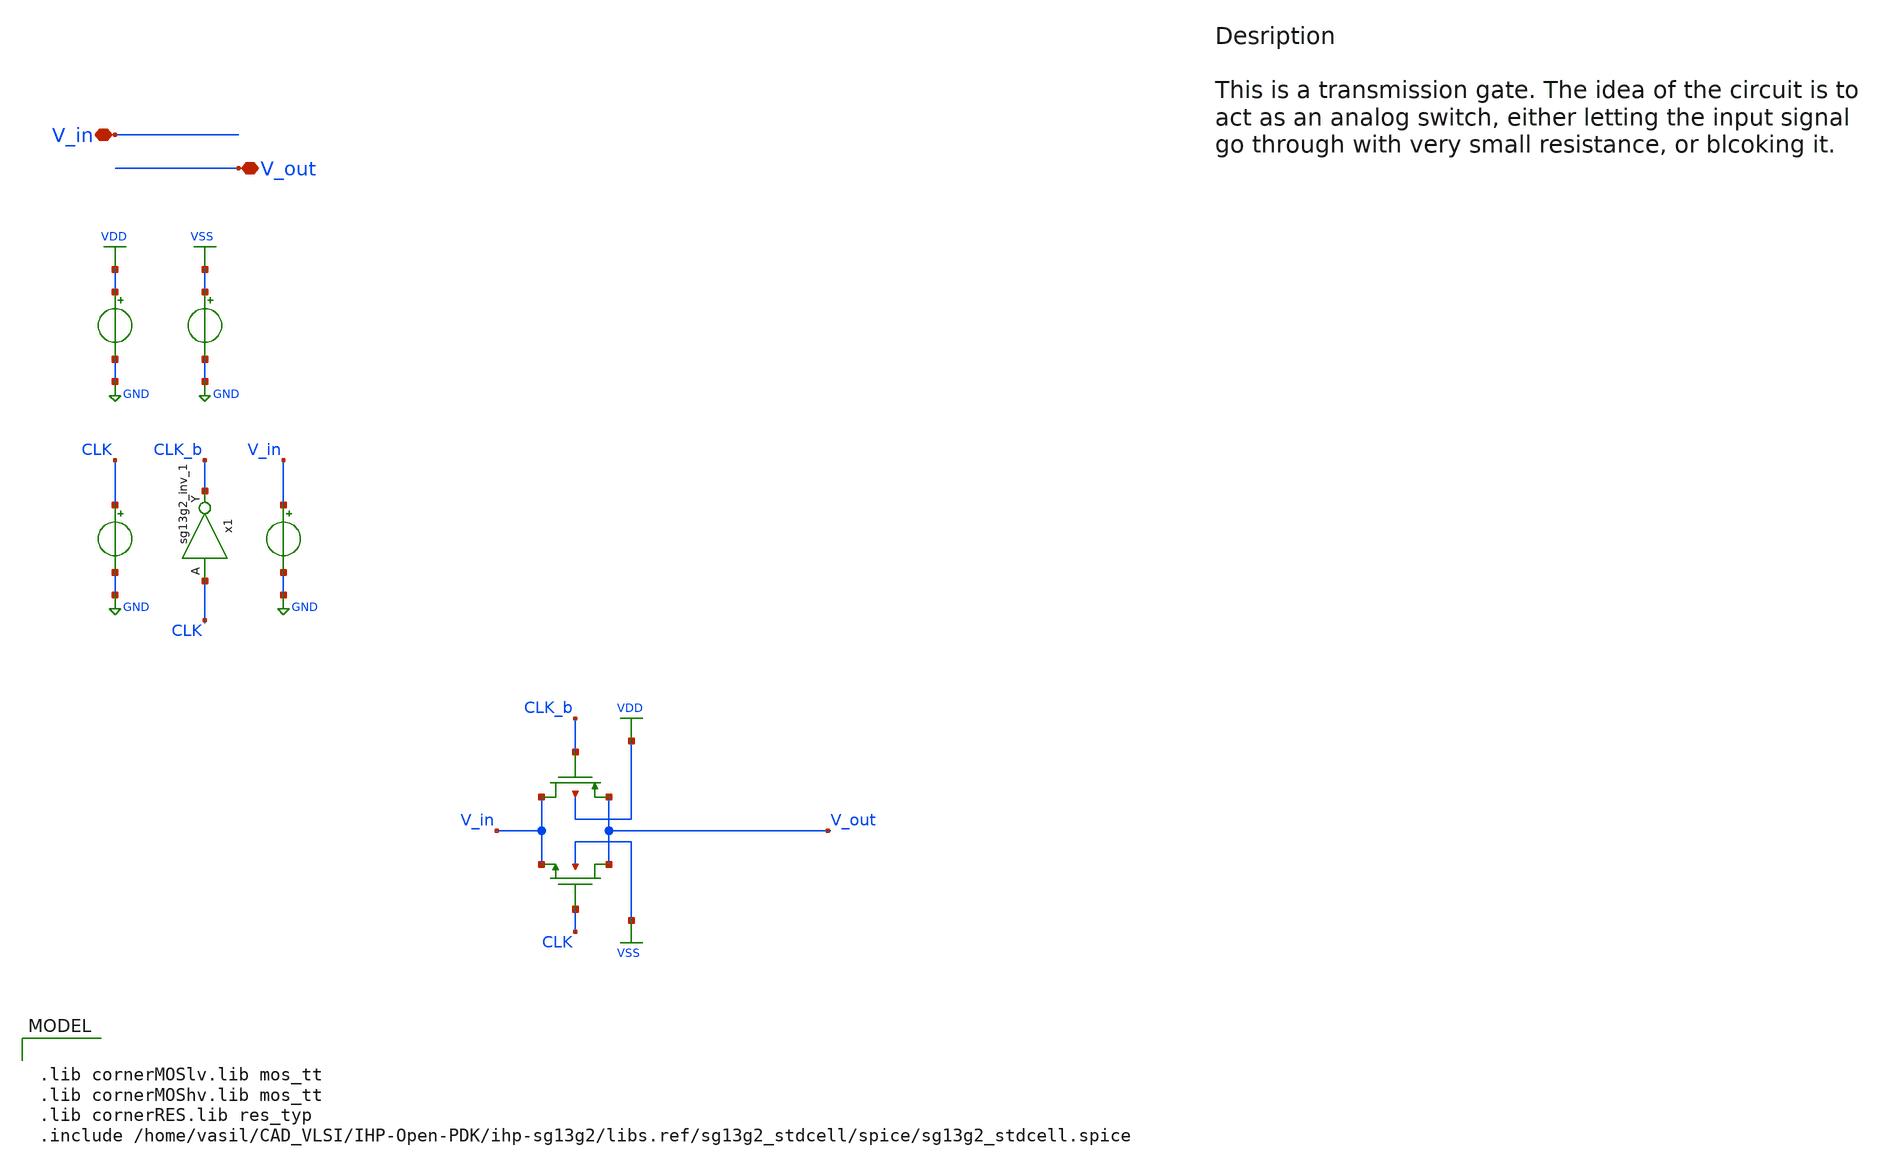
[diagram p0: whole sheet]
** sch_path: CKT_14/xschem/circuit_14.sch
**.subckt circuit_14 V_in V_out
*.iopin V_in
*.iopin V_out
XM1 V_in CLK_b V_out VDD sg13_lv_pmos w=1.0u l=0.45u ng=1 m=1 mm_ok=1
XM2 V_out CLK V_in VSS sg13_lv_nmos w=1.0u l=0.45u ng=1 m=1 mm_ok=1
V1 CLK GND pulse (0 1.5 0.5n 100p 100p 1n 2.2n)
.save i(v1)
V2 VDD GND 1.5
.save i(v2)
V3 VSS GND 0
.save i(v3)
vin V_in GND 0.8
.save i(vin)
x1 CLK_b CLK VDD VSS sg13g2_inv_1
**** begin user architecture code

.lib cornerMOSlv.lib mos_tt
.lib cornerMOShv.lib mos_tt
.lib cornerRES.lib res_typ
.include /home/vasil/CAD_VLSI/IHP-Open-PDK/ihp-sg13g2/libs.ref/sg13g2_stdcell/spice/sg13g2_stdcell.spice



.temp 27
.param vin=0
.control
dc vin 0 1.5 0.01
write circuit_14_dc.raw

tran 1p 10n
write circuit_14_tran.raw
.endc




.save all


**** end user architecture code
**.ends

* expanding   symbol:  sg13g2_stdcells/sg13g2_inv_1.sym # of pins=2
** sym_path: sg13g2_stdcells/sg13g2_inv_1.sym
** sch_path: sg13g2_stdcells/sg13g2_inv_1.sch
.subckt sg13g2_inv_1 Y A VDD VSS
*.opin Y
*.ipin A
*.iopin VDD
*.iopin VSS
XM1 Y A VSS VSS sg13_lv_nmos w=740.00n l=130.00n ng=1 m=1 mm_ok=1
XM2 Y A VDD VDD sg13_lv_pmos w=1.12u l=130.00n ng=1 m=1 mm_ok=1
.ends

.GLOBAL GND
.GLOBAL VDD
.GLOBAL VSS
.end
